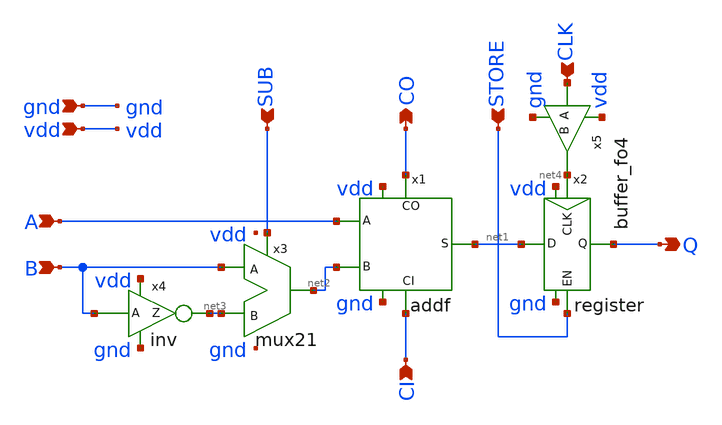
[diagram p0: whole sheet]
** sch_path: xschem/bitslice.sch
**.subckt bitslice A B CI CLK STORE CO Q SUB vdd gnd
*.ipin A
*.ipin B
*.ipin CI
*.ipin CLK
*.ipin STORE
*.opin CO
*.opin Q
*.ipin SUB
*.ipin vdd
*.ipin gnd
x1 A net2 CI net1 CO vdd gnd addf
x2 net4 STORE Q net1 vdd gnd register
x3 SUB B net2 net3 mux21
x4 net3 B vdd gnd inv
x5 net4 CLK vdd gnd buffer_fo4
**.ends
.end
